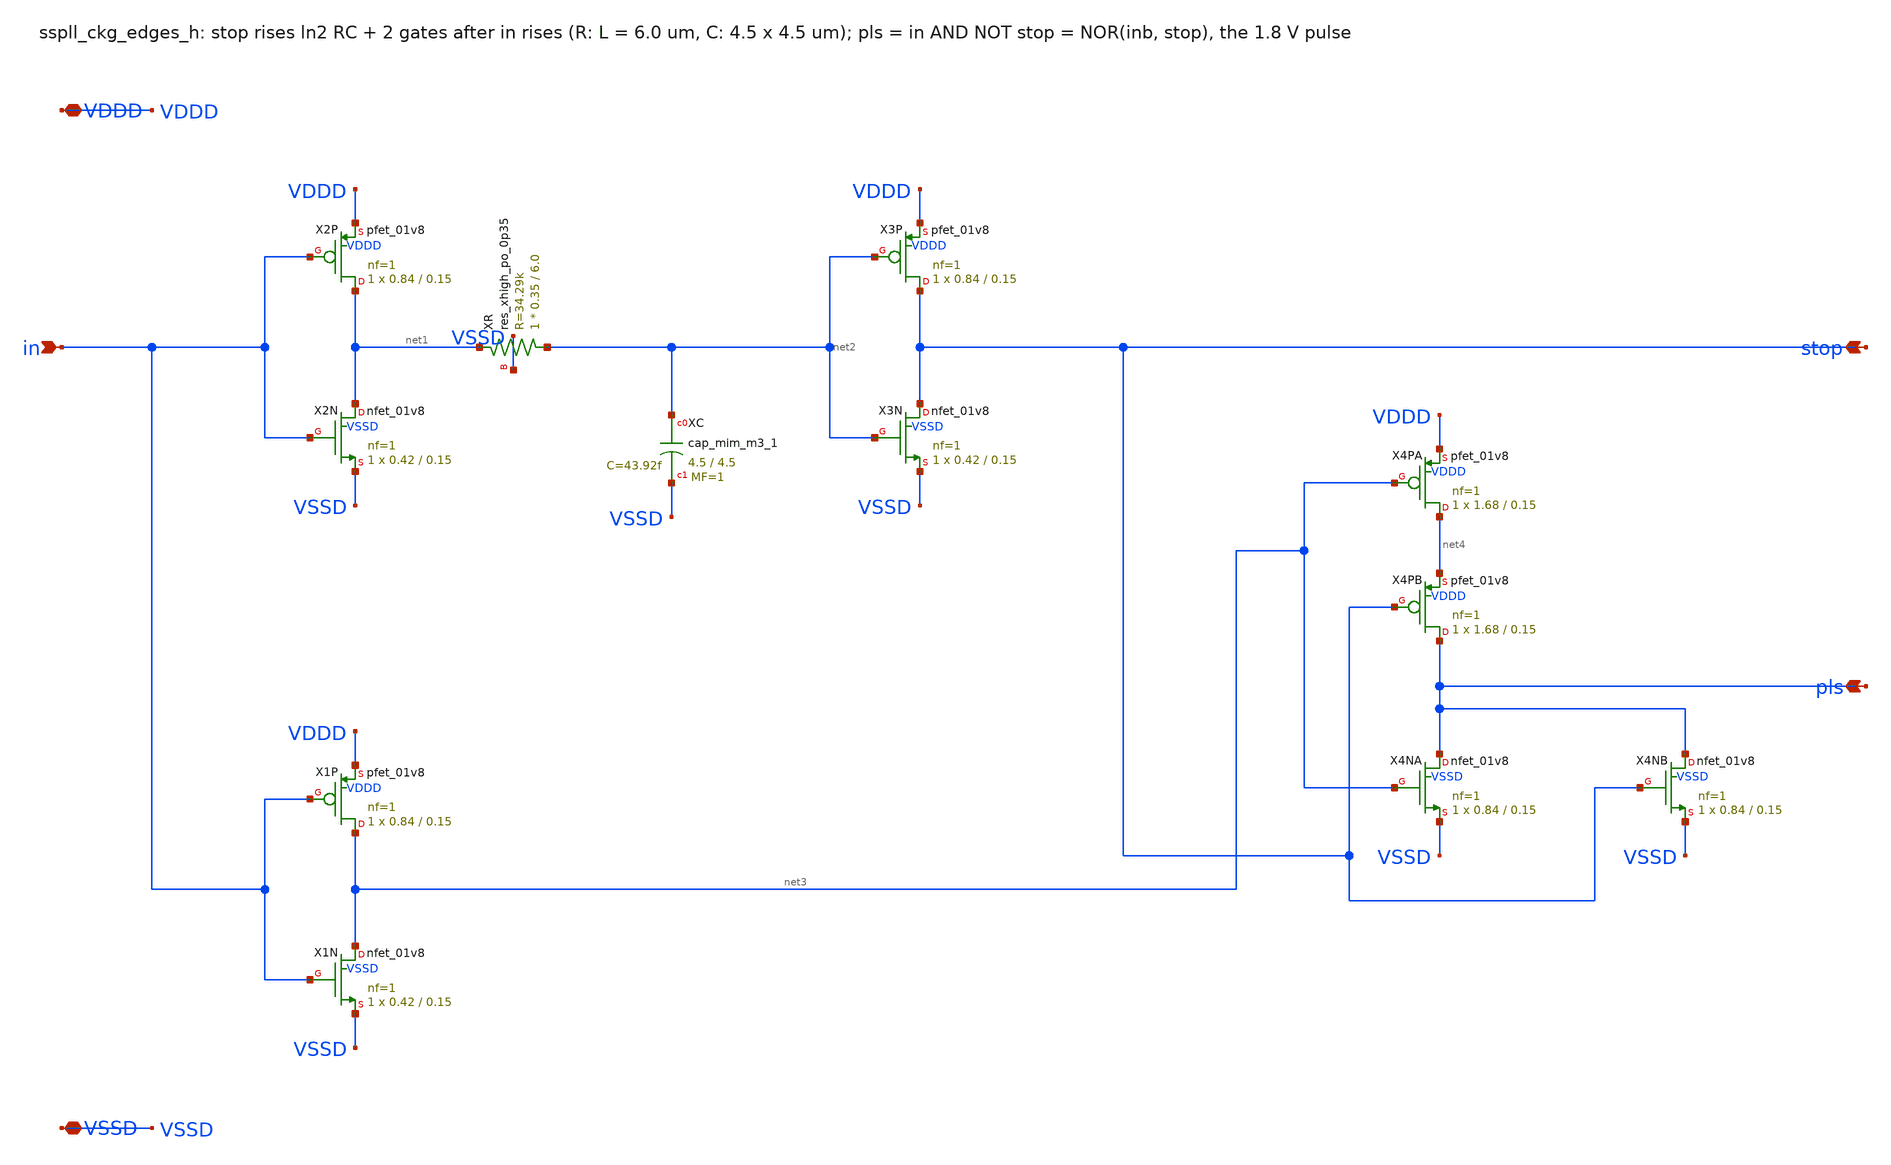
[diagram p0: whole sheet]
** sch_path: xschem/clkgen_hv/sspll_ckg_edges_h.sch
**.subckt sspll_ckg_edges_h in stop pls VDDD VSSD
*.ipin in
*.opin stop
*.opin pls
*.iopin VDDD
*.iopin VSSD
XX2P net1 in VDDD VDDD sky130_fd_pr__pfet_01v8 L=0.15 W=0.84 nf=1 ad='int((nf+1)/2) * W/nf * 0.29' as='int((nf+2)/2) * W/nf * 0.29'
+ pd='2*int((nf+1)/2) * (W/nf + 0.29)' ps='2*int((nf+2)/2) * (W/nf + 0.29)' nrd='0.29 / W' nrs='0.29 / W'
+ sa=0 sb=0 sd=0 mult=1 m=1
XX2N net1 in VSSD VSSD sky130_fd_pr__nfet_01v8 L=0.15 W=0.42 nf=1 ad='int((nf+1)/2) * W/nf * 0.29' as='int((nf+2)/2) * W/nf * 0.29'
+ pd='2*int((nf+1)/2) * (W/nf + 0.29)' ps='2*int((nf+2)/2) * (W/nf + 0.29)' nrd='0.29 / W' nrs='0.29 / W'
+ sa=0 sb=0 sd=0 mult=1 m=1
XXR net2 net1 VSSD sky130_fd_pr__res_xhigh_po_0p35 L=6.0 mult=1 m=1
XXC net2 VSSD sky130_fd_pr__cap_mim_m3_1 W=4.5 L=4.5 MF=1 m=1
XX3P stop net2 VDDD VDDD sky130_fd_pr__pfet_01v8 L=0.15 W=0.84 nf=1 ad='int((nf+1)/2) * W/nf * 0.29'
+ as='int((nf+2)/2) * W/nf * 0.29' pd='2*int((nf+1)/2) * (W/nf + 0.29)' ps='2*int((nf+2)/2) * (W/nf + 0.29)'
+ nrd='0.29 / W' nrs='0.29 / W' sa=0 sb=0 sd=0 mult=1 m=1
XX3N stop net2 VSSD VSSD sky130_fd_pr__nfet_01v8 L=0.15 W=0.42 nf=1 ad='int((nf+1)/2) * W/nf * 0.29'
+ as='int((nf+2)/2) * W/nf * 0.29' pd='2*int((nf+1)/2) * (W/nf + 0.29)' ps='2*int((nf+2)/2) * (W/nf + 0.29)'
+ nrd='0.29 / W' nrs='0.29 / W' sa=0 sb=0 sd=0 mult=1 m=1
XX1P net3 in VDDD VDDD sky130_fd_pr__pfet_01v8 L=0.15 W=0.84 nf=1 ad='int((nf+1)/2) * W/nf * 0.29' as='int((nf+2)/2) * W/nf * 0.29'
+ pd='2*int((nf+1)/2) * (W/nf + 0.29)' ps='2*int((nf+2)/2) * (W/nf + 0.29)' nrd='0.29 / W' nrs='0.29 / W'
+ sa=0 sb=0 sd=0 mult=1 m=1
XX1N net3 in VSSD VSSD sky130_fd_pr__nfet_01v8 L=0.15 W=0.42 nf=1 ad='int((nf+1)/2) * W/nf * 0.29' as='int((nf+2)/2) * W/nf * 0.29'
+ pd='2*int((nf+1)/2) * (W/nf + 0.29)' ps='2*int((nf+2)/2) * (W/nf + 0.29)' nrd='0.29 / W' nrs='0.29 / W'
+ sa=0 sb=0 sd=0 mult=1 m=1
XX4PA net4 net3 VDDD VDDD sky130_fd_pr__pfet_01v8 L=0.15 W=1.68 nf=1 ad='int((nf+1)/2) * W/nf * 0.29'
+ as='int((nf+2)/2) * W/nf * 0.29' pd='2*int((nf+1)/2) * (W/nf + 0.29)' ps='2*int((nf+2)/2) * (W/nf + 0.29)'
+ nrd='0.29 / W' nrs='0.29 / W' sa=0 sb=0 sd=0 mult=1 m=1
XX4PB pls stop net4 VDDD sky130_fd_pr__pfet_01v8 L=0.15 W=1.68 nf=1 ad='int((nf+1)/2) * W/nf * 0.29'
+ as='int((nf+2)/2) * W/nf * 0.29' pd='2*int((nf+1)/2) * (W/nf + 0.29)' ps='2*int((nf+2)/2) * (W/nf + 0.29)'
+ nrd='0.29 / W' nrs='0.29 / W' sa=0 sb=0 sd=0 mult=1 m=1
XX4NA pls net3 VSSD VSSD sky130_fd_pr__nfet_01v8 L=0.15 W=0.84 nf=1 ad='int((nf+1)/2) * W/nf * 0.29'
+ as='int((nf+2)/2) * W/nf * 0.29' pd='2*int((nf+1)/2) * (W/nf + 0.29)' ps='2*int((nf+2)/2) * (W/nf + 0.29)'
+ nrd='0.29 / W' nrs='0.29 / W' sa=0 sb=0 sd=0 mult=1 m=1
XX4NB pls stop VSSD VSSD sky130_fd_pr__nfet_01v8 L=0.15 W=0.84 nf=1 ad='int((nf+1)/2) * W/nf * 0.29'
+ as='int((nf+2)/2) * W/nf * 0.29' pd='2*int((nf+1)/2) * (W/nf + 0.29)' ps='2*int((nf+2)/2) * (W/nf + 0.29)'
+ nrd='0.29 / W' nrs='0.29 / W' sa=0 sb=0 sd=0 mult=1 m=1
**.ends
.end
